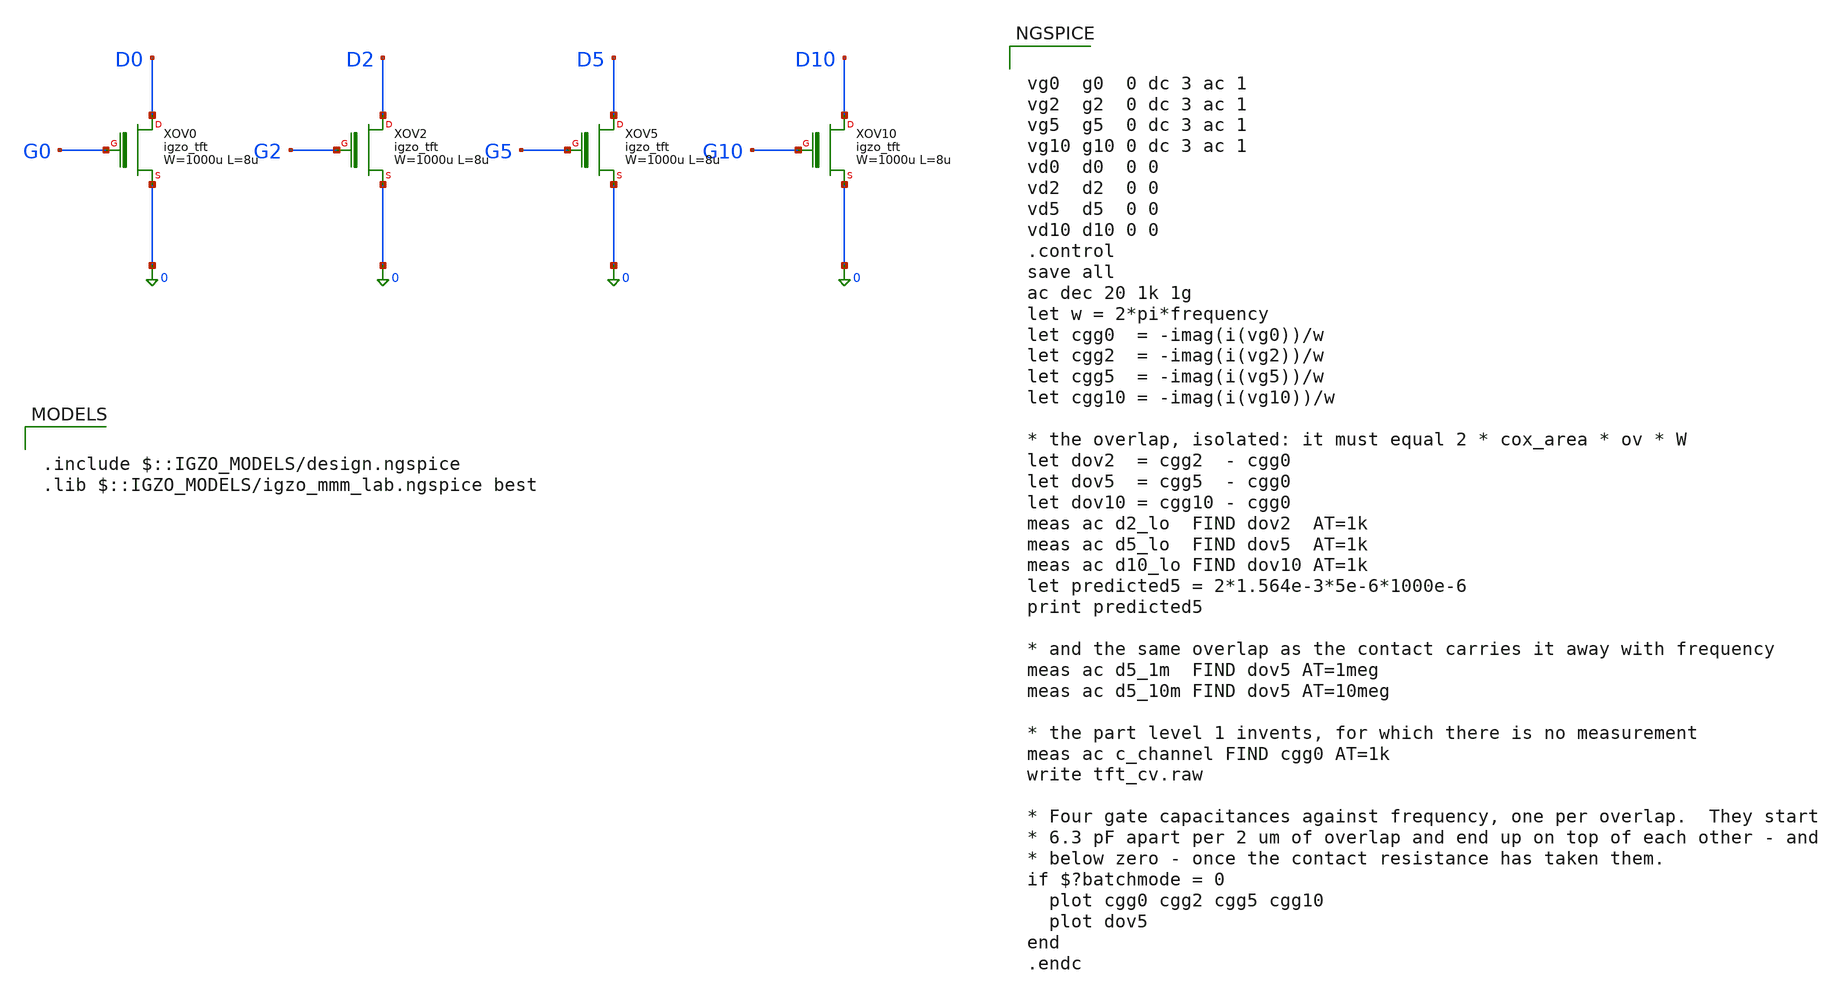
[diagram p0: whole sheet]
** sch_path: libs.tech/xschem/tests/tft_cv.sch
**.subckt tft_cv
XXOV0 D0 G0 0 igzo_tft W=1000u L=8u ov=0 nf=1 m=1
XXOV2 D2 G2 0 igzo_tft W=1000u L=8u ov=2u nf=1 m=1
XXOV5 D5 G5 0 igzo_tft W=1000u L=8u ov=5u nf=1 m=1
XXOV10 D10 G10 0 igzo_tft W=1000u L=8u ov=10u nf=1 m=1
**** begin user architecture code

.include $::IGZO_MODELS/design.ngspice
.lib $::IGZO_MODELS/igzo_mmm_lab.ngspice best



vg0  g0  0 dc 3 ac 1
vg2  g2  0 dc 3 ac 1
vg5  g5  0 dc 3 ac 1
vg10 g10 0 dc 3 ac 1
vd0  d0  0 0
vd2  d2  0 0
vd5  d5  0 0
vd10 d10 0 0
.control
save all
ac dec 20 1k 1g
let w = 2*pi*frequency
let cgg0  = -imag(i(vg0))/w
let cgg2  = -imag(i(vg2))/w
let cgg5  = -imag(i(vg5))/w
let cgg10 = -imag(i(vg10))/w

* the overlap, isolated: it must equal 2 * cox_area * ov * W
let dov2  = cgg2  - cgg0
let dov5  = cgg5  - cgg0
let dov10 = cgg10 - cgg0
meas ac d2_lo  FIND dov2  AT=1k
meas ac d5_lo  FIND dov5  AT=1k
meas ac d10_lo FIND dov10 AT=1k
let predicted5 = 2*1.564e-3*5e-6*1000e-6
print predicted5

* and the same overlap as the contact carries it away with frequency
meas ac d5_1m  FIND dov5 AT=1meg
meas ac d5_10m FIND dov5 AT=10meg

* the part level 1 invents, for which there is no measurement
meas ac c_channel FIND cgg0 AT=1k
write tft_cv.raw

* Four gate capacitances against frequency, one per overlap.  They start
* 6.3 pF apart per 2 um of overlap and end up on top of each other - and
* below zero - once the contact resistance has taken them.
if $?batchmode = 0
  plot cgg0 cgg2 cgg5 cgg10
  plot dov5
end
.endc


**** end user architecture code
**.ends
.end
